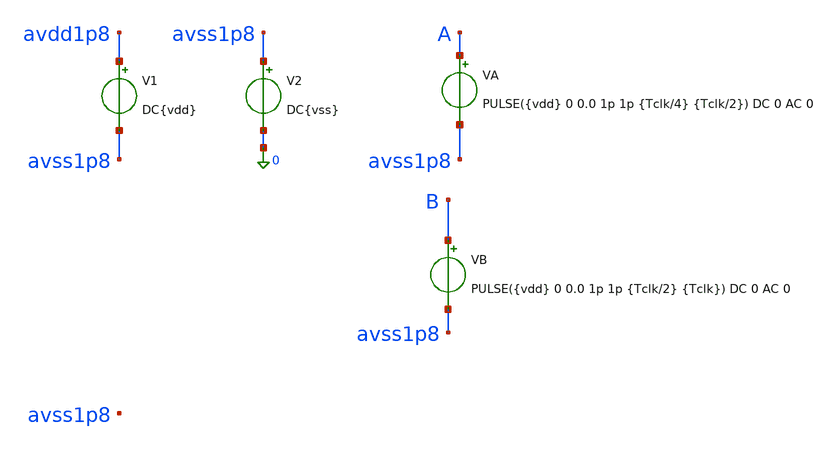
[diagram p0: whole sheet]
** sch_path: verification/testbenches/nand/tb_nand.sch
**.subckt tb_nand
V1 avdd1p8 avss1p8 DC{vdd}
V2 avss1p8 0 DC{vss}
VA A avss1p8 PULSE({vdd} 0 0.0 1p 1p {Tclk/4} {Tclk/2}) DC 0 AC 0
VB B avss1p8 PULSE({vdd} 0 0.0 1p 1p {Tclk/2} {Tclk}) DC 0 AC 0
**** begin user architecture code


* Circuit Parameters
.param vdd = 1.2
.param vss = 0.0
.param Tclk = 10n
.options TEMP = 27.0
* Include Models - IHP SG13G2
.lib cornerMOSlv.lib mos_tt
* OP Parameters & Singals to save
.save all
*Simulations
.control
tran 0.01u 100n
setplot tran1
plot v(OUT)
reset
.endc
.end


**** end user architecture code
**.ends
.end
